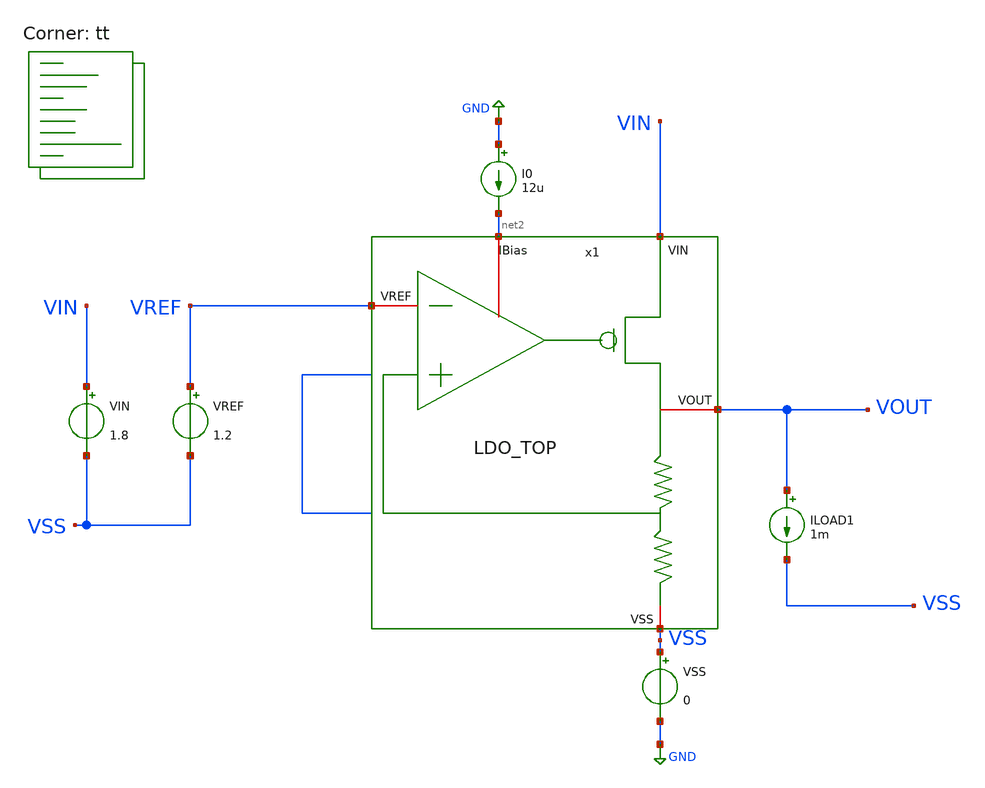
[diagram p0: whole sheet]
** sch_path: LDO_1p5V/tests/LDR.sch
**.subckt LDR
VSS VSS GND 0
VREF VREF VSS 1.2
VIN VIN VSS 1.8
I0 GND net2 12u
ILOAD1 VOUT VSS 1m
x1 VIN net2 VREF VOUT VSS LDO_TOP
**** begin user architecture code


.options savecurrents
.save all

.control
set filetype=ascii

echo ===== LOAD REGULATION ANALYSIS =====

* Mantén VIN fijo en el valor típico
alter VIN 1.8

* Barrido de corriente de carga: 10uA a 1mA
dc ILOAD1 10u 1m 10u

echo ===== MEASUREMENTS =====

meas dc vout_min min v(VOUT)
meas dc vout_max max v(VOUT)

let delta_vout = vout_max - vout_min
let delta_iload = 1m - 10u

* Load regulation en V/A
let load_reg_v_a = delta_vout / delta_iload

* Load regulation en mV/mA
let load_reg_mv_ma = load_reg_v_a

* Variación total de salida en mV
let load_reg_total_mv = delta_vout * 1000

echo ===== LOAD REGULATION RESULTS =====
print vout_min
print vout_max
print delta_vout
print load_reg_mv_ma
print load_reg_total_mv

plot v(VOUT)

.endc


.lib $::SKYWATER_MODELS/sky130.lib.spice tt
**** end user architecture code
**.ends

* expanding   symbol:  /foss/designs/Curso_Semiconductores/LDO_1p5V/schematics/LDO_TOP.sym # of
*+ pins=5
** sym_path: LDO/LDO_TOP.sym
** sch_path: LDO/LDO_TOP.sch
.subckt LDO_TOP VIN IBias VREF VOUT VSS
*.iopin VIN
*.iopin VREF
*.iopin IBias
*.iopin VOUT
*.iopin VSS
x1 VIN IBias VREF VOUT net1 net1 VSS LDO
.ends


* expanding   symbol:  /foss/designs/Curso_Semiconductores/LDO/LDO.sym # of pins=7
** sym_path: LDO/LDO.sym
** sch_path: LDO/LDO.sch
.subckt LDO VIN IBias VREF VOUT VFB1 VFB2 VSS
*.iopin VIN
*.iopin VREF
*.iopin VFB1
*.iopin VSS
*.iopin VFB2
*.iopin VOUT
*.iopin IBias
XM7 VOUT Vgate VIN VIN sky130_fd_pr__pfet_01v8 L=0.15 W=6 nf=1 ad='int((1 + 1)/2) * 6 / 1 * 0.29' as='int((1 + 2)/2) * 6 / 1 * 0.29'
+ pd='2*int((1 + 1)/2) * (6 / 1 + 0.29)' ps='2*int((1 + 2)/2) * (6 / 1 + 0.29)' nrd='0.29 / 6 ' nrs='0.29 / 6 '
+ sa=0 sb=0 sd=0 mult=50 m=50
XC3 Vgate VOUT sky130_fd_pr__model__cap_mim W=10 L=10 MF=1 m=1
x1 VIN Vgate VREF VFB1 IBias VSS OTA_5T
x2 VOUT VFB2 VSS RES_FB
.ends


* expanding   symbol:  /foss/designs/Curso_Semiconductores/OTA_5T/OTA_5T.sym # of pins=6
** sym_path: /foss/designs/Curso_Semiconductores/OTA_5T/OTA_5T.sym
** sch_path: /foss/designs/Curso_Semiconductores/OTA_5T/OTA_5T.sch
.subckt OTA_5T VIN VOUT_AMP VINN VINP IB VSS
*.iopin VIN
*.iopin VSS
*.iopin VOUT_AMP
*.iopin IB
*.iopin VINN
*.iopin VINP
XM1 IB IB VSS VSS sky130_fd_pr__nfet_01v8 L=1 W=2.5 nf=1 ad='int((1 + 1)/2) * 2.5 / 1 * 0.29' as='int((1 + 2)/2) * 2.5 / 1 * 0.29'
+ pd='2*int((1 + 1)/2) * (2.5 / 1 + 0.29)' ps='2*int((1 + 2)/2) * (2.5 / 1 + 0.29)' nrd='0.29 / 2.5 ' nrs='0.29 / 2.5 '
+ sa=0 sb=0 sd=0 mult=4 m=4
XM2 tail IB VSS VSS sky130_fd_pr__nfet_01v8 L=1 W=2.5 nf=1 ad='int((1 + 1)/2) * 2.5 / 1 * 0.29' as='int((1 + 2)/2) * 2.5 / 1 * 0.29'
+ pd='2*int((1 + 1)/2) * (2.5 / 1 + 0.29)' ps='2*int((1 + 2)/2) * (2.5 / 1 + 0.29)' nrd='0.29 / 2.5 ' nrs='0.29 / 2.5 '
+ sa=0 sb=0 sd=0 mult=4 m=4
XM3 net1 VINP tail VSS sky130_fd_pr__nfet_01v8 L=1 W=3 nf=1 ad='int((1 + 1)/2) * 3 / 1 * 0.29' as='int((1 + 2)/2) * 3 / 1 * 0.29'
+ pd='2*int((1 + 1)/2) * (3 / 1 + 0.29)' ps='2*int((1 + 2)/2) * (3 / 1 + 0.29)' nrd='0.29 / 3 ' nrs='0.29 / 3 '
+ sa=0 sb=0 sd=0 mult=4 m=4
XM4 VOUT_AMP VINN tail VSS sky130_fd_pr__nfet_01v8 L=1 W=3 nf=1 ad='int((1 + 1)/2) * 3 / 1 * 0.29' as='int((1 + 2)/2) * 3 / 1 * 0.29'
+ pd='2*int((1 + 1)/2) * (3 / 1 + 0.29)' ps='2*int((1 + 2)/2) * (3 / 1 + 0.29)' nrd='0.29 / 3 ' nrs='0.29 / 3 '
+ sa=0 sb=0 sd=0 mult=4 m=4
XM5 VOUT_AMP net1 VIN VIN sky130_fd_pr__pfet_01v8 L=1 W=6 nf=1 ad='int((1 + 1)/2) * 6 / 1 * 0.29' as='int((1 + 2)/2) * 6 / 1 * 0.29'
+ pd='2*int((1 + 1)/2) * (6 / 1 + 0.29)' ps='2*int((1 + 2)/2) * (6 / 1 + 0.29)' nrd='0.29 / 6 ' nrs='0.29 / 6 '
+ sa=0 sb=0 sd=0 mult=4 m=4
XM6 net1 net1 VIN VIN sky130_fd_pr__pfet_01v8 L=1 W=6 nf=1 ad='int((1 + 1)/2) * 6 / 1 * 0.29' as='int((1 + 2)/2) * 6 / 1 * 0.29'
+ pd='2*int((1 + 1)/2) * (6 / 1 + 0.29)' ps='2*int((1 + 2)/2) * (6 / 1 + 0.29)' nrd='0.29 / 6 ' nrs='0.29 / 6 '
+ sa=0 sb=0 sd=0 mult=4 m=4
XD tail VSS tail VSS sky130_fd_pr__nfet_01v8 L=0.15 W=3 nf=1 ad='int((1 + 1)/2) * 3 / 1 * 0.29' as='int((1 + 2)/2) * 3 / 1 * 0.29'
+ pd='2*int((1 + 1)/2) * (3 / 1 + 0.29)' ps='2*int((1 + 2)/2) * (3 / 1 + 0.29)' nrd='0.29 / 3 ' nrs='0.29 / 3 '
+ sa=0 sb=0 sd=0 mult=4 m=4
XM7 VIN VIN VIN VIN sky130_fd_pr__pfet_01v8 L=0.15 W=6 nf=1 ad='int((1 + 1)/2) * 6 / 1 * 0.29' as='int((1 + 2)/2) * 6 / 1 * 0.29'
+ pd='2*int((1 + 1)/2) * (6 / 1 + 0.29)' ps='2*int((1 + 2)/2) * (6 / 1 + 0.29)' nrd='0.29 / 6 ' nrs='0.29 / 6 '
+ sa=0 sb=0 sd=0 mult=4 m=4
.ends


* expanding   symbol:  /foss/designs/Curso_Semiconductores/RES_FB/RES_FB.sym # of pins=3
** sym_path: RES_FB/RES_FB.sym
** sch_path: RES_FB/RES_FB.sch
.subckt RES_FB VOUT VFB VSS
*.iopin VOUT
*.iopin VFB
*.iopin VSS
XR11 net1 VOUT VSS sky130_fd_pr__res_xhigh_po_0p69 L=8.62 mult=1 m=1
XR1 VFB net1 VSS sky130_fd_pr__res_xhigh_po_0p69 L=8.62 mult=1 m=1
XR2 net8 VFB VSS sky130_fd_pr__res_xhigh_po_0p69 L=8.62 mult=1 m=1
XR3 net4 net8 VSS sky130_fd_pr__res_xhigh_po_0p69 L=8.62 mult=1 m=1
XR4 net2 net4 VSS sky130_fd_pr__res_xhigh_po_0p69 L=8.62 mult=1 m=1
XR5 net5 net2 VSS sky130_fd_pr__res_xhigh_po_0p69 L=8.62 mult=1 m=1
XR6 net3 net5 VSS sky130_fd_pr__res_xhigh_po_0p69 L=8.62 mult=1 m=1
XR7 net7 net3 VSS sky130_fd_pr__res_xhigh_po_0p69 L=8.62 mult=1 m=1
XR8 net6 net7 VSS sky130_fd_pr__res_xhigh_po_0p69 L=8.62 mult=1 m=1
XR9 VSS net6 VSS sky130_fd_pr__res_xhigh_po_0p69 L=8.62 mult=1 m=1
.ends

.GLOBAL GND
.end
